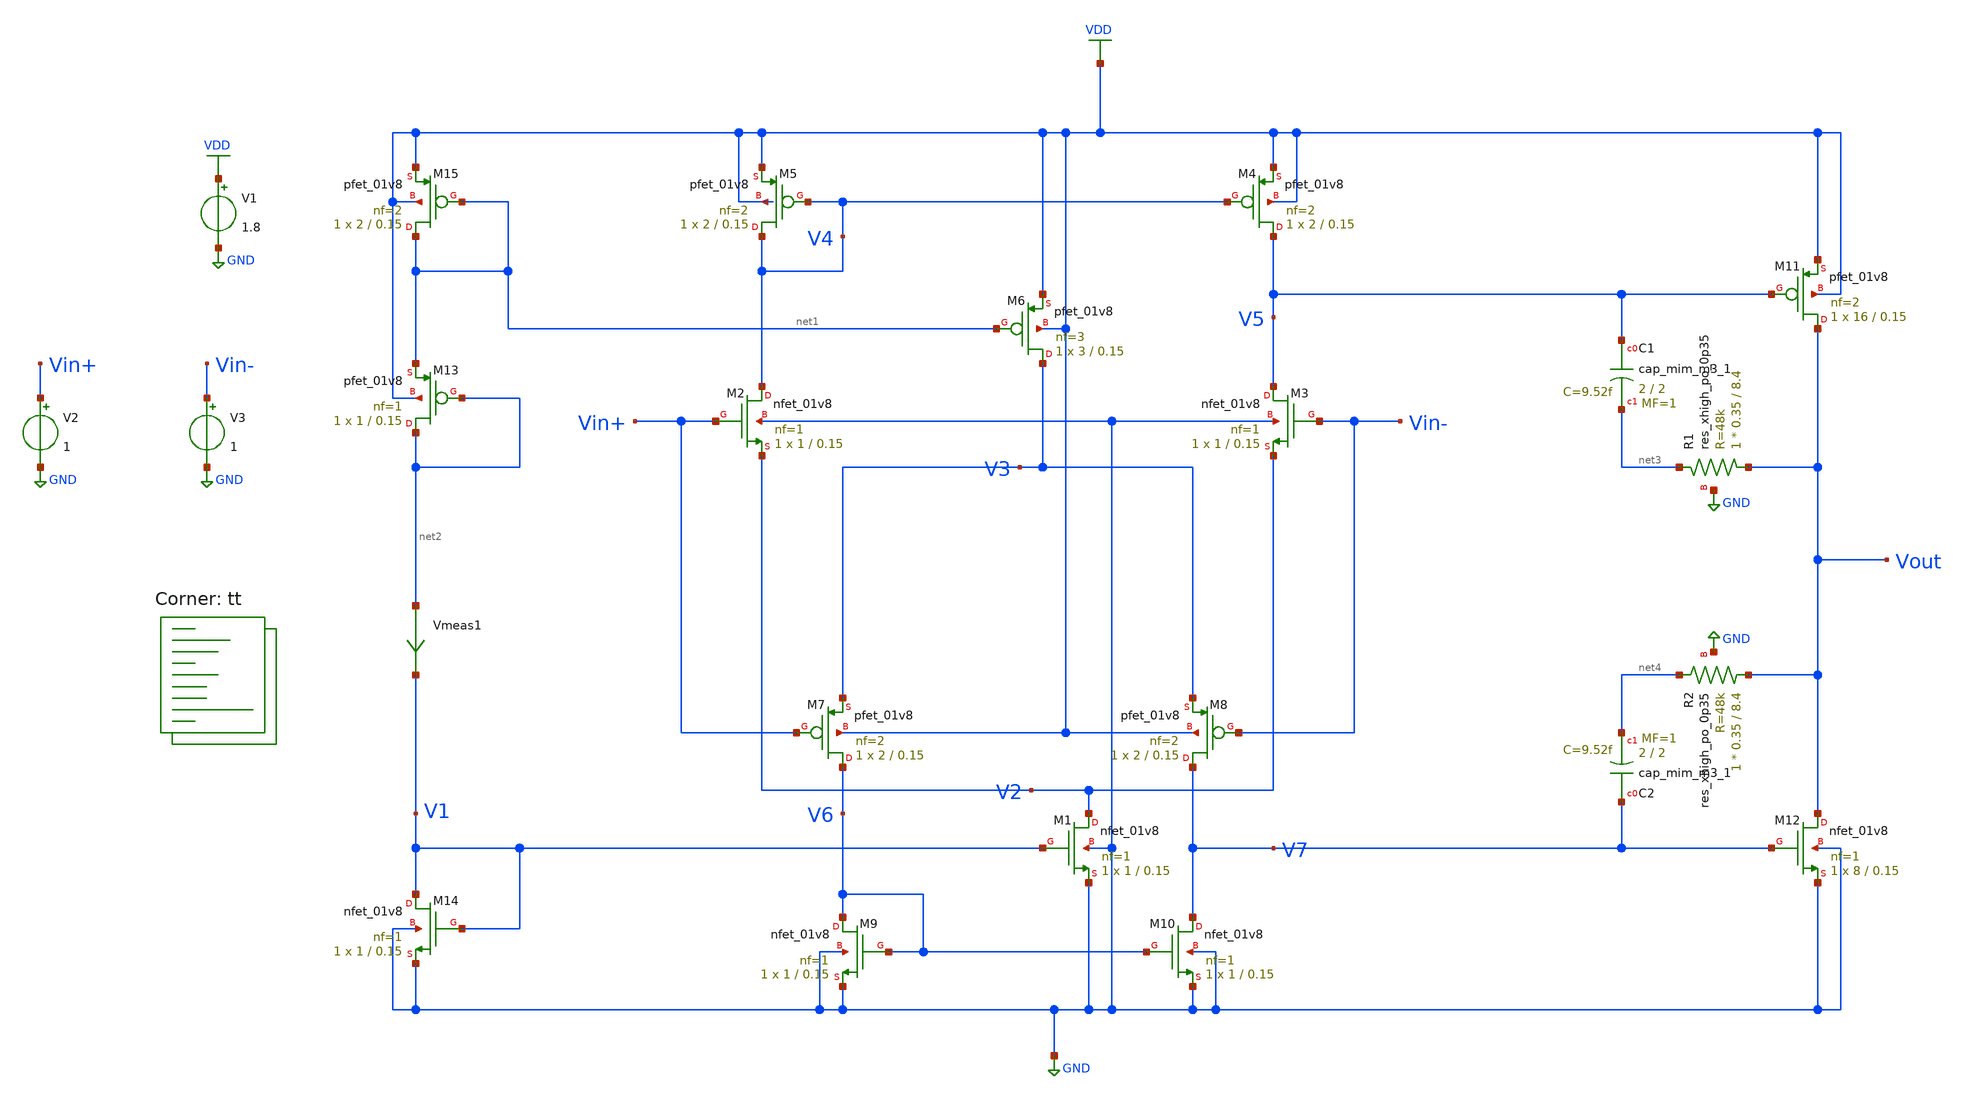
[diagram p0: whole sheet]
** sch_path: projects/pll/charge_pump/xschem_ngspice/tb_rail_to_rail_opamp5.sch
**.subckt tb_rail_to_rail_opamp5
V1 VDD GND 1.8
V2 Vin+ GND 1
V3 Vin- GND 1
XM2 V4 Vin+ V2 GND sky130_fd_pr__nfet_01v8 L=0.15 W=1 nf=1 ad='int((nf+1)/2) * W/nf * 0.29' as='int((nf+2)/2) * W/nf * 0.29'
+ pd='2*int((nf+1)/2) * (W/nf + 0.29)' ps='2*int((nf+2)/2) * (W/nf + 0.29)' nrd='0.29 / W' nrs='0.29 / W'
+ sa=0 sb=0 sd=0 mult=1 m=1
XM3 V5 Vin- V2 GND sky130_fd_pr__nfet_01v8 L=0.15 W=1 nf=1 ad='int((nf+1)/2) * W/nf * 0.29' as='int((nf+2)/2) * W/nf * 0.29'
+ pd='2*int((nf+1)/2) * (W/nf + 0.29)' ps='2*int((nf+2)/2) * (W/nf + 0.29)' nrd='0.29 / W' nrs='0.29 / W'
+ sa=0 sb=0 sd=0 mult=1 m=1
XM5 V4 V4 VDD VDD sky130_fd_pr__pfet_01v8 L=0.15 W=2 nf=2 ad='int((nf+1)/2) * W/nf * 0.29' as='int((nf+2)/2) * W/nf * 0.29'
+ pd='2*int((nf+1)/2) * (W/nf + 0.29)' ps='2*int((nf+2)/2) * (W/nf + 0.29)' nrd='0.29 / W' nrs='0.29 / W'
+ sa=0 sb=0 sd=0 mult=1 m=1
XM4 V5 V4 VDD VDD sky130_fd_pr__pfet_01v8 L=0.15 W=2 nf=2 ad='int((nf+1)/2) * W/nf * 0.29' as='int((nf+2)/2) * W/nf * 0.29'
+ pd='2*int((nf+1)/2) * (W/nf + 0.29)' ps='2*int((nf+2)/2) * (W/nf + 0.29)' nrd='0.29 / W' nrs='0.29 / W'
+ sa=0 sb=0 sd=0 mult=1 m=1
XM6 V3 net1 VDD VDD sky130_fd_pr__pfet_01v8 L=0.15 W=3 nf=3 ad='int((nf+1)/2) * W/nf * 0.29' as='int((nf+2)/2) * W/nf * 0.29'
+ pd='2*int((nf+1)/2) * (W/nf + 0.29)' ps='2*int((nf+2)/2) * (W/nf + 0.29)' nrd='0.29 / W' nrs='0.29 / W'
+ sa=0 sb=0 sd=0 mult=1 m=1
XM7 V6 Vin+ V3 VDD sky130_fd_pr__pfet_01v8 L=0.15 W=2 nf=2 ad='int((nf+1)/2) * W/nf * 0.29' as='int((nf+2)/2) * W/nf * 0.29'
+ pd='2*int((nf+1)/2) * (W/nf + 0.29)' ps='2*int((nf+2)/2) * (W/nf + 0.29)' nrd='0.29 / W' nrs='0.29 / W'
+ sa=0 sb=0 sd=0 mult=1 m=1
XM8 V7 Vin- V3 VDD sky130_fd_pr__pfet_01v8 L=0.15 W=2 nf=2 ad='int((nf+1)/2) * W/nf * 0.29' as='int((nf+2)/2) * W/nf * 0.29'
+ pd='2*int((nf+1)/2) * (W/nf + 0.29)' ps='2*int((nf+2)/2) * (W/nf + 0.29)' nrd='0.29 / W' nrs='0.29 / W'
+ sa=0 sb=0 sd=0 mult=1 m=1
XM9 V6 V6 GND GND sky130_fd_pr__nfet_01v8 L=0.15 W=1 nf=1 ad='int((nf+1)/2) * W/nf * 0.29' as='int((nf+2)/2) * W/nf * 0.29'
+ pd='2*int((nf+1)/2) * (W/nf + 0.29)' ps='2*int((nf+2)/2) * (W/nf + 0.29)' nrd='0.29 / W' nrs='0.29 / W'
+ sa=0 sb=0 sd=0 mult=1 m=1
XM10 V7 V6 GND GND sky130_fd_pr__nfet_01v8 L=0.15 W=1 nf=1 ad='int((nf+1)/2) * W/nf * 0.29' as='int((nf+2)/2) * W/nf * 0.29'
+ pd='2*int((nf+1)/2) * (W/nf + 0.29)' ps='2*int((nf+2)/2) * (W/nf + 0.29)' nrd='0.29 / W' nrs='0.29 / W'
+ sa=0 sb=0 sd=0 mult=1 m=1
XM1 V2 V1 GND GND sky130_fd_pr__nfet_01v8 L=0.15 W=1 nf=1 ad='int((nf+1)/2) * W/nf * 0.29' as='int((nf+2)/2) * W/nf * 0.29'
+ pd='2*int((nf+1)/2) * (W/nf + 0.29)' ps='2*int((nf+2)/2) * (W/nf + 0.29)' nrd='0.29 / W' nrs='0.29 / W'
+ sa=0 sb=0 sd=0 mult=1 m=1
XM11 Vout V5 VDD VDD sky130_fd_pr__pfet_01v8 L=0.15 W=16 nf=2 ad='int((nf+1)/2) * W/nf * 0.29' as='int((nf+2)/2) * W/nf * 0.29'
+ pd='2*int((nf+1)/2) * (W/nf + 0.29)' ps='2*int((nf+2)/2) * (W/nf + 0.29)' nrd='0.29 / W' nrs='0.29 / W'
+ sa=0 sb=0 sd=0 mult=1 m=1
XM12 Vout V7 GND GND sky130_fd_pr__nfet_01v8 L=0.15 W=8 nf=1 ad='int((nf+1)/2) * W/nf * 0.29' as='int((nf+2)/2) * W/nf * 0.29'
+ pd='2*int((nf+1)/2) * (W/nf + 0.29)' ps='2*int((nf+2)/2) * (W/nf + 0.29)' nrd='0.29 / W' nrs='0.29 / W'
+ sa=0 sb=0 sd=0 mult=1 m=1
XM14 V1 V1 GND GND sky130_fd_pr__nfet_01v8 L=0.15 W=1 nf=1 ad='int((nf+1)/2) * W/nf * 0.29' as='int((nf+2)/2) * W/nf * 0.29'
+ pd='2*int((nf+1)/2) * (W/nf + 0.29)' ps='2*int((nf+2)/2) * (W/nf + 0.29)' nrd='0.29 / W' nrs='0.29 / W'
+ sa=0 sb=0 sd=0 mult=1 m=1
XM15 net1 net1 VDD VDD sky130_fd_pr__pfet_01v8 L=0.15 W=2 nf=2 ad='int((nf+1)/2) * W/nf * 0.29' as='int((nf+2)/2) * W/nf * 0.29'
+ pd='2*int((nf+1)/2) * (W/nf + 0.29)' ps='2*int((nf+2)/2) * (W/nf + 0.29)' nrd='0.29 / W' nrs='0.29 / W'
+ sa=0 sb=0 sd=0 mult=1 m=1
Vmeas1 net2 V1 0
.save i(vmeas1)
XM13 net2 net2 net1 VDD sky130_fd_pr__pfet_01v8 L=0.15 W=1 nf=1 ad='int((nf+1)/2) * W/nf * 0.29' as='int((nf+2)/2) * W/nf * 0.29'
+ pd='2*int((nf+1)/2) * (W/nf + 0.29)' ps='2*int((nf+2)/2) * (W/nf + 0.29)' nrd='0.29 / W' nrs='0.29 / W'
+ sa=0 sb=0 sd=0 mult=1 m=1
XC1 V5 net3 sky130_fd_pr__cap_mim_m3_1 W=2 L=2 MF=1 m=1
XR1 Vout net3 GND sky130_fd_pr__res_xhigh_po_0p35 L=8.4 mult=1 m=1
XC2 V7 net4 sky130_fd_pr__cap_mim_m3_1 W=2 L=2 MF=1 m=1
XR2 Vout net4 GND sky130_fd_pr__res_xhigh_po_0p35 L=8.4 mult=1 m=1
**** begin user architecture code



.option wnflag=1
* .option savecurrents

* .param VDDGAUSS = agauss(1.8, 0.05, 1)
* .param VDD = VDDGAUSS
* .param VDD = 1.8

* .param TEMPGAUSS = agauss(40, 30, 1)
* .param temp = TEMPGAUSS
* .option temp = 26

.save @m.xm1.msky130_fd_pr__nfet_01v8[gm] @m.xm2.msky130_fd_pr__nfet_01v8[gm] @m.xm3.msky130_fd_pr__nfet_01v8[gm] @m.xm4.msky130_fd_pr__pfet_01v8[gm] @m.xm5.msky130_fd_pr__pfet_01v8[gm] @m.xm6.msky130_fd_pr__pfet_01v8[gm] @m.xm7.msky130_fd_pr__pfet_01v8[gm] @m.xm8.msky130_fd_pr__pfet_01v8[gm] @m.xm9.msky130_fd_pr__nfet_01v8[gm] @m.xm10.msky130_fd_pr__nfet_01v8[gm] @m.xm11.msky130_fd_pr__pfet_01v8[gm] @m.xm12.msky130_fd_pr__nfet_01v8[gm] @m.xm13.msky130_fd_pr__nfet_01v8[gm] @m.xm14.msky130_fd_pr__nfet_01v8[gm] @m.xm15.msky130_fd_pr__pfet_01v8[gm]


.control
*let i_start = 0
*let i_stop = 2u
 * dowhile i_start <= i_stop
  *  alter IREF $&i_start
    save all
  * tran 50p 2u
  * ac dec 20 1 1T
  dc V2 0 1.8 0.01
  write tb_rail_to_rail_opamp5.raw
  * write tb_rail_to_rail_opamp5_AC.raw
    set appendwrite
  * reset
  * let i_start = i_start + 0.1u
 * end
.endc



.lib $::SKYWATER_MODELS/sky130.lib.spice tt
**** end user architecture code
**.ends
.GLOBAL GND
.GLOBAL VDD
.end
